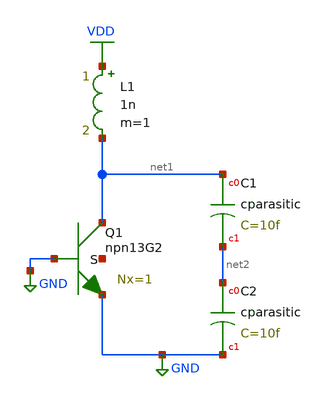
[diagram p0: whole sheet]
** sch_path: exp/IHP130/vco/sch/vco.sch
**.subckt vco
XQ1 net1 GND GND net3 npn13G2 Nx=1 mm_ok=1
XC1 net1 net2 cparasitic C=10f
L1 VDD net1 1n m=1
XC2 net2 GND cparasitic C=10f
**.ends
.GLOBAL GND
.GLOBAL VDD
.end
